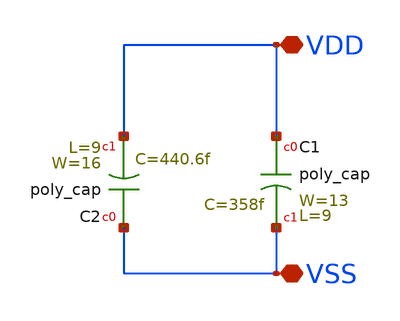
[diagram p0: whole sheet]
** sch_path: design/xschem/VCO/SA_VCO_DECAP_B.sch
**.subckt SA_VCO_DECAP_B VDD VSS
*.iopin VDD
*.iopin VSS
C1 VDD VSS poly_cap W=13 L=9
C2 VSS VDD poly_cap W=16 L=9
**.ends
.end
